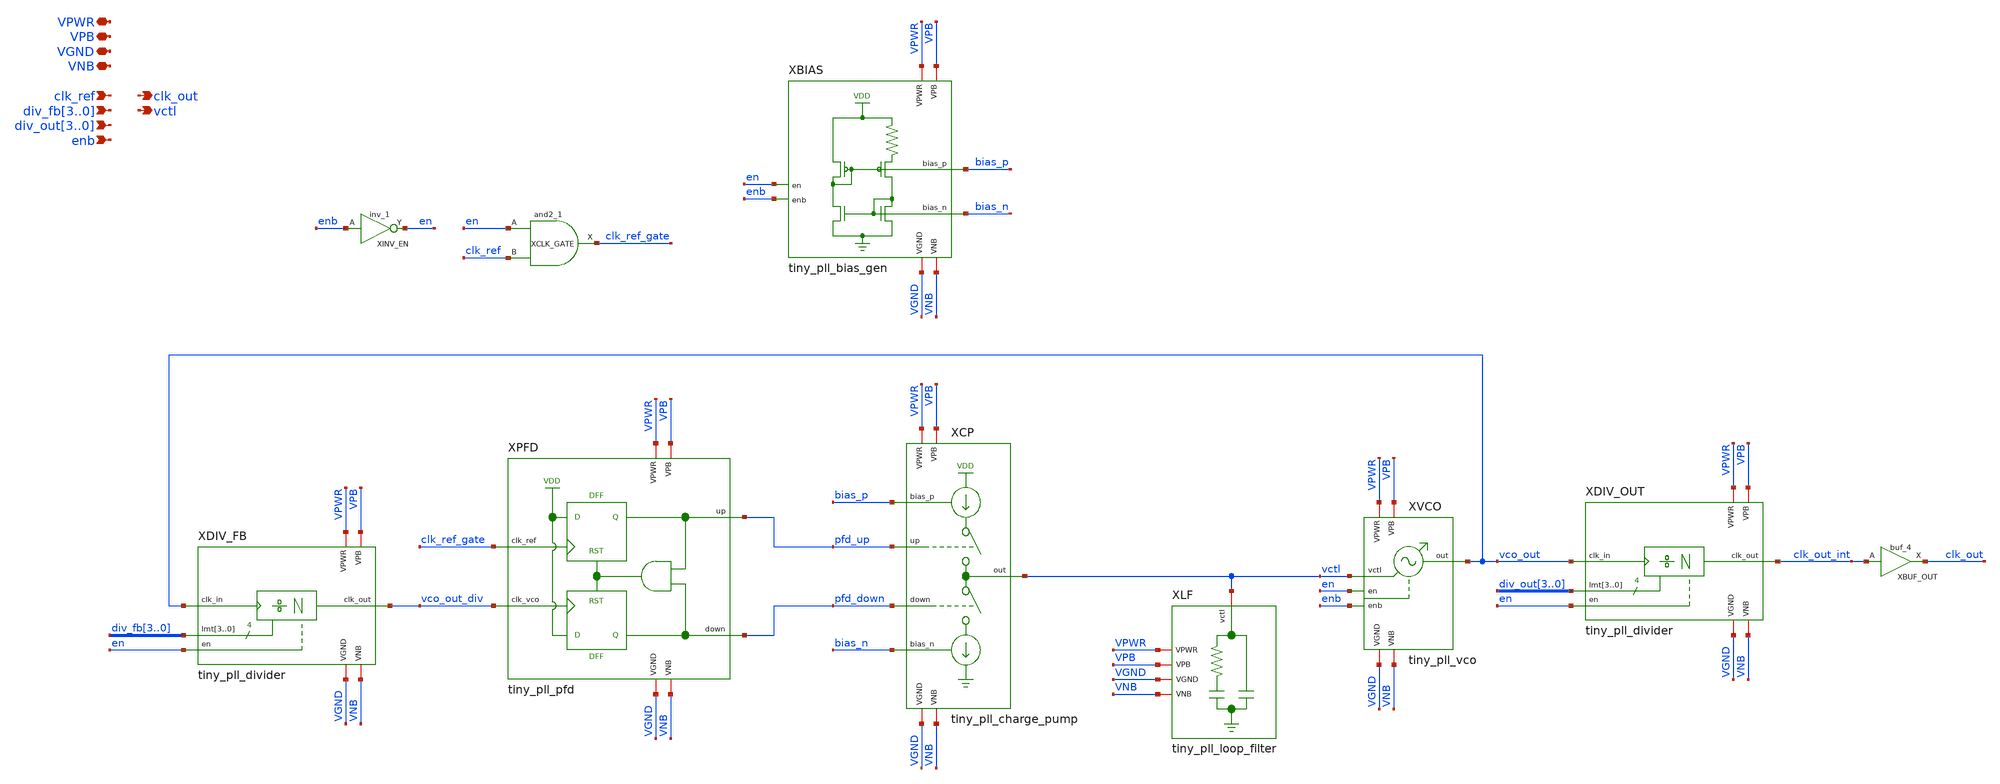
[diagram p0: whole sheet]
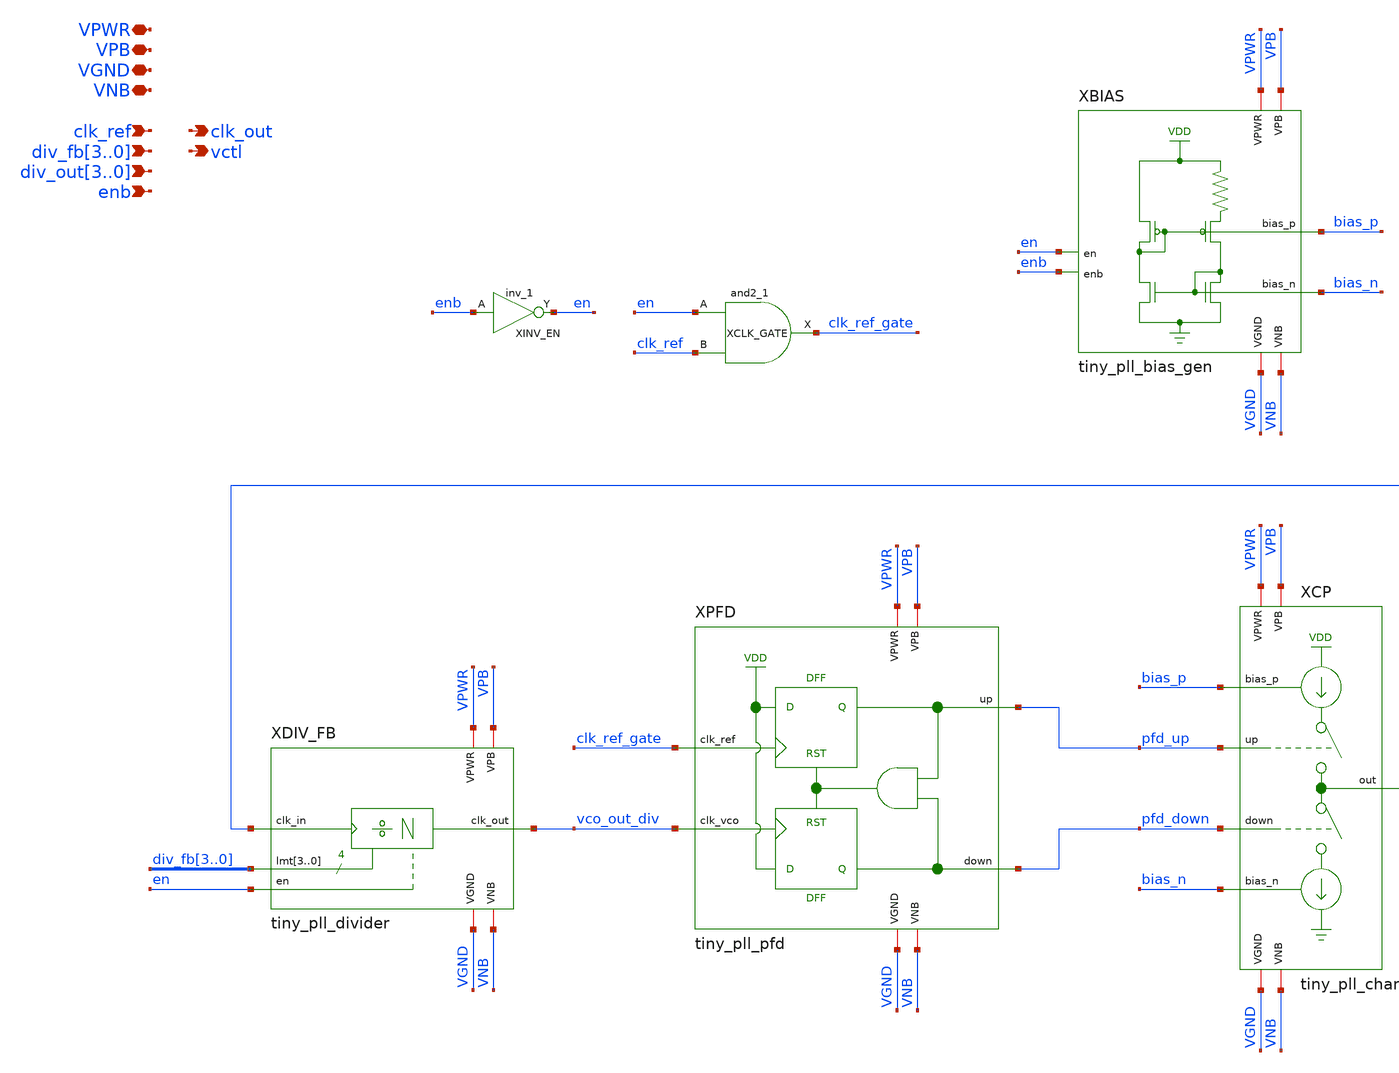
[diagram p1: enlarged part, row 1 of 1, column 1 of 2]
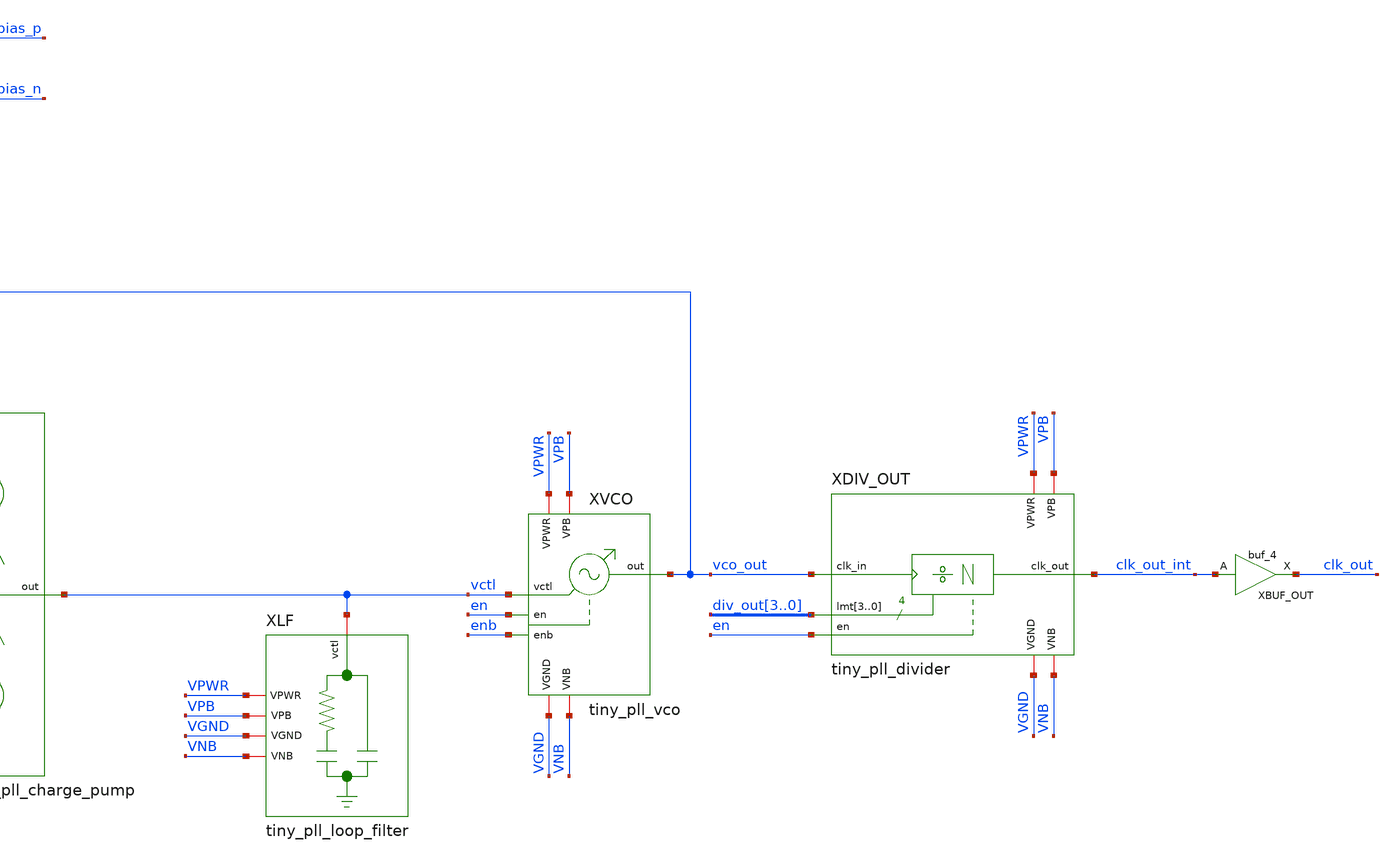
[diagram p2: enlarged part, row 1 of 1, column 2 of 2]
** sch_path: xschem/tiny_pll/tiny_pll.sch
**.subckt tiny_pll clk_ref clk_out VPWR VPB VGND VNB div_fb3,div_fb2,div_fb1,div_fb0
*+ div_out3,div_out2,div_out1,div_out0 enb vctl
*.ipin clk_ref
*.opin clk_out
*.iopin VPWR
*.iopin VPB
*.iopin VGND
*.iopin VNB
*.ipin div_fb3,div_fb2,div_fb1,div_fb0
*.ipin div_out3,div_out2,div_out1,div_out0
*.ipin enb
*.opin vctl
XVCO VPWR VPB VGND VNB vco_out vctl en enb tiny_pll_vco
XCP VPWR VPB VGND VNB vctl pfd_up pfd_down bias_n bias_p tiny_pll_charge_pump
XDIV_OUT VPWR VPB VGND VNB clk_out_int vco_out div_out3 div_out2 div_out1 div_out0 en
+ tiny_pll_divider
XPFD VPWR VPB VGND VNB pfd_up clk_ref_gate pfd_down vco_out_div tiny_pll_pfd
XDIV_FB VPWR VPB VGND VNB vco_out_div vco_out div_fb3 div_fb2 div_fb1 div_fb0 en tiny_pll_divider
XLF VGND VNB VPWR VPB vctl tiny_pll_loop_filter
XBIAS VGND VNB VPWR VPB bias_n en enb bias_p tiny_pll_bias_gen
XINV_EN enb VGND VNB VPB VPWR en sky130_fd_sc_hd__inv_1
XBUF_OUT clk_out_int VGND VNB VPB VPWR clk_out sky130_fd_sc_hd__buf_4
XCLK_GATE en clk_ref VGND VNB VPB VPWR clk_ref_gate sky130_fd_sc_hd__and2_1
**.ends
.end
